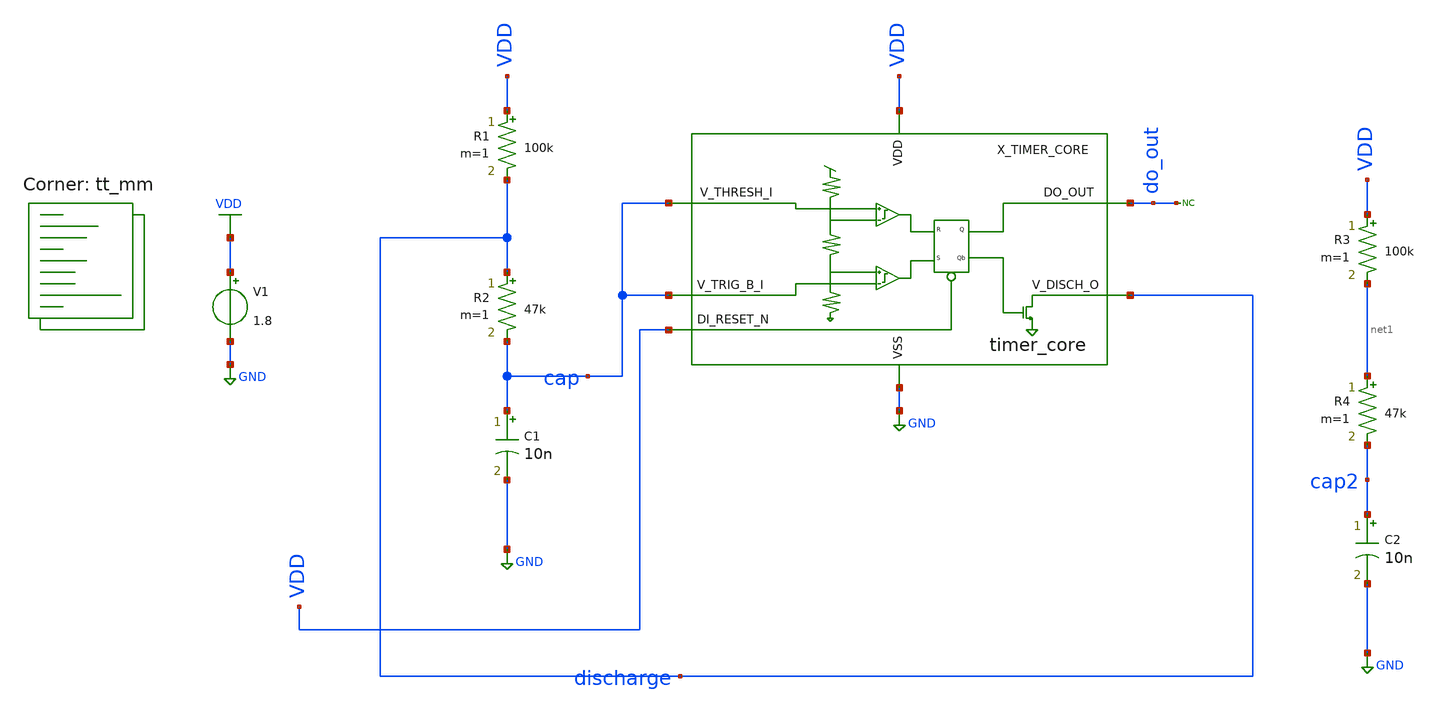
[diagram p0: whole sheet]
** sch_path: xsch/tb/timer_core/tb_timer_core_astable_mc.sch
**.subckt tb_timer_core_astable_mc
V1 VDD GND 1.8
R1 VDD discharge 100k m=1
R2 discharge cap 47k m=1
C1 cap GND 10n m=1
* noconn do_out
R3 VDD net1 100k m=1
R4 net1 cap2 47k m=1
C2 cap2 GND 10n m=1
X_TIMER_CORE cap cap VDD do_out discharge VDD GND timer_core
**** begin user architecture code


.ic v(cap) = 0
.ic v(cap2) = 0

.control

set singlescale
set wr_vecnames

let mc_runs = 4
let run = 0
let period = vector(mc_runs)
let duty = vector(mc_runs)
let fr = vector(mc_runs)
let design_point = vector(mc_runs)

while run <= mc_runs

	tran 1u 10m
	;plot v(do_out) v(cap)

	meas tran thigh trig v(do_out) val=0.9 rise=3 targ v(do_out) val=0.9 fall=4
	meas tran tlow trig v(do_out) val=0.9 fall=4 targ v(do_out) val=0.9 rise=4

	let period[run] = thigh+tlow
	let duty[run] = thigh/period[run];
	let fr[run] = 1/period[run];

	echo Period: $&period
	echo Frequency: $&fr
	echo Duty Cycle: $&duty

	reset
	let run = run + 1;
end

plot tran1.v(cap) tran2.v(cap) tran3.v(cap) tran4.v(cap)
wrdata tb_timer_core_astable_frequency_vs_designpoint.txt fr vs design_point
.endc
.end


.lib $::SKYWATER_MODELS/sky130.lib.spice tt_mm


.save v(do_out) v(discharge) v(cap) v(x_timer_core.out_inv3) v(cap2)

.savecurrents


**** end user architecture code
**.ends
.GLOBAL VDD
.GLOBAL GND
.end
